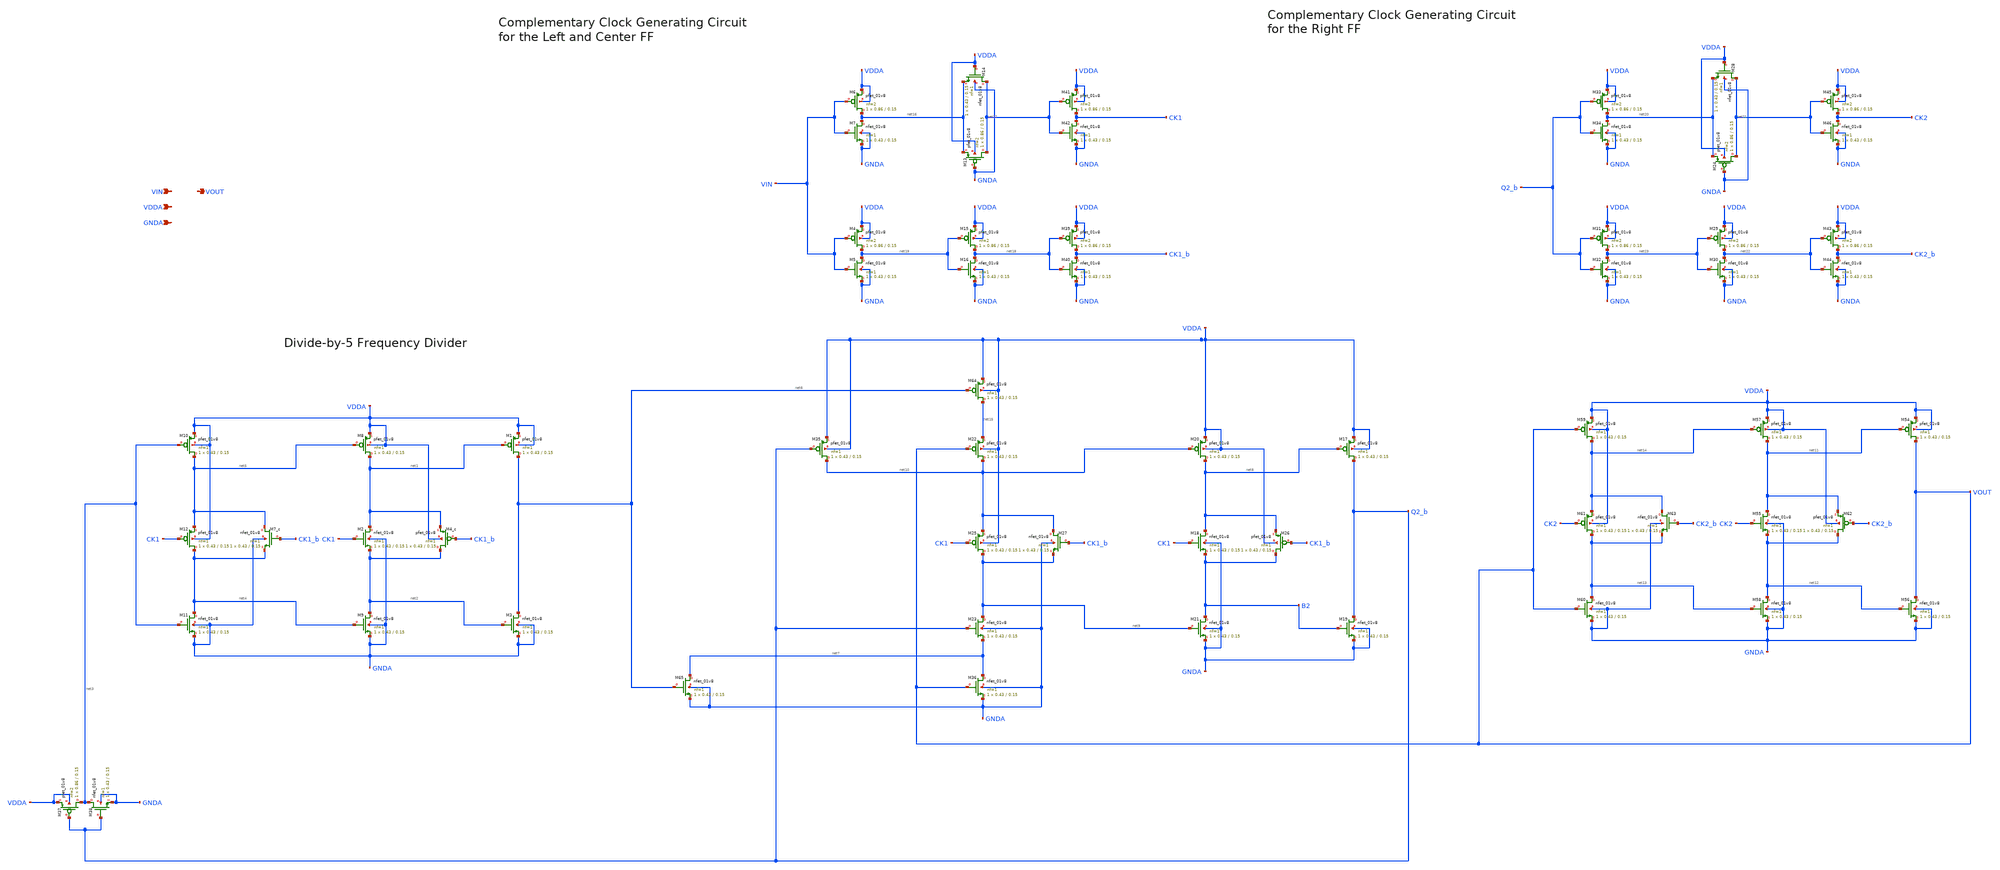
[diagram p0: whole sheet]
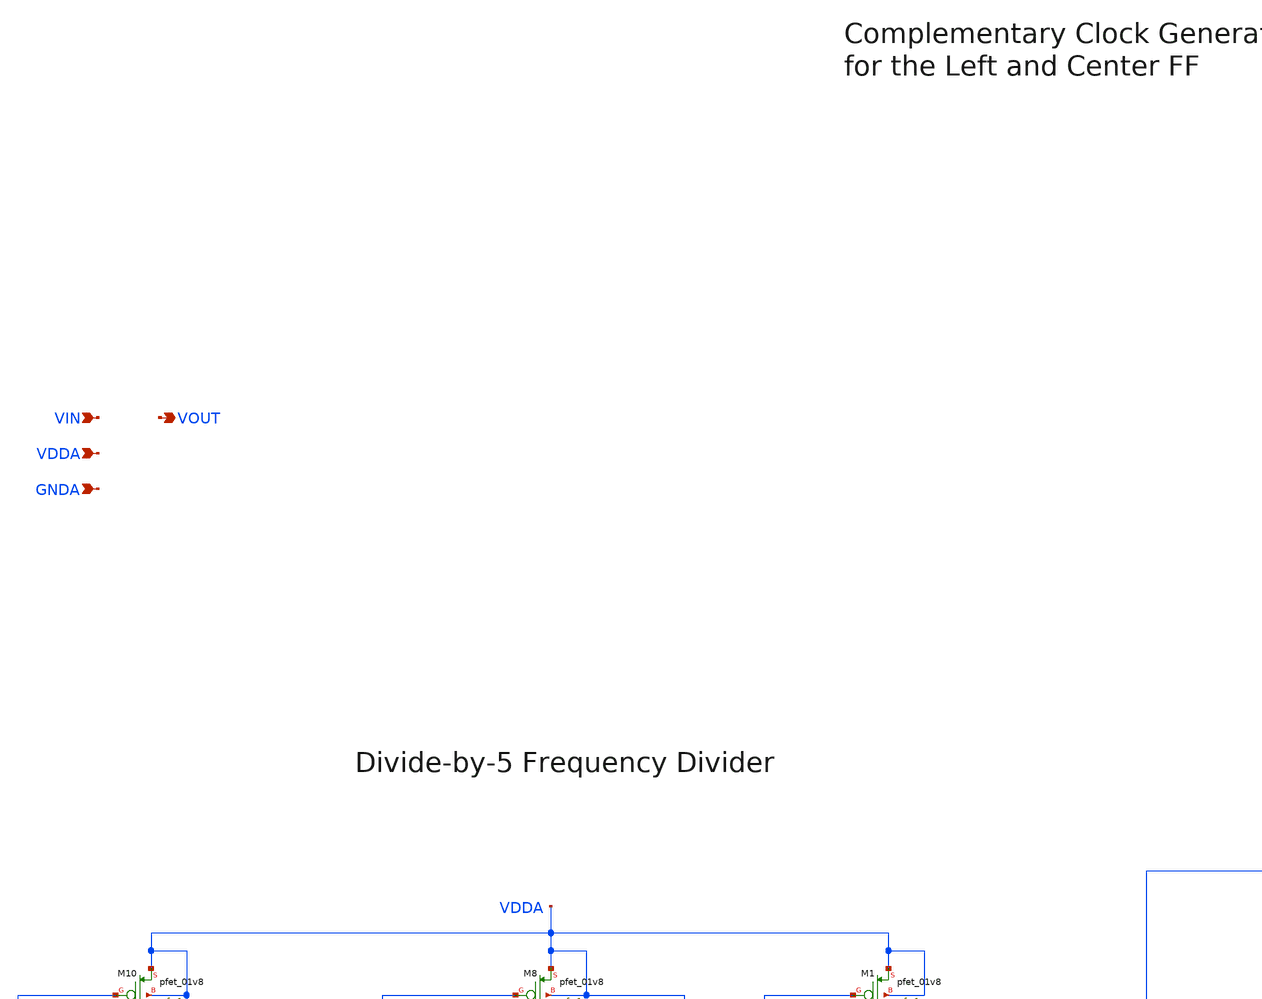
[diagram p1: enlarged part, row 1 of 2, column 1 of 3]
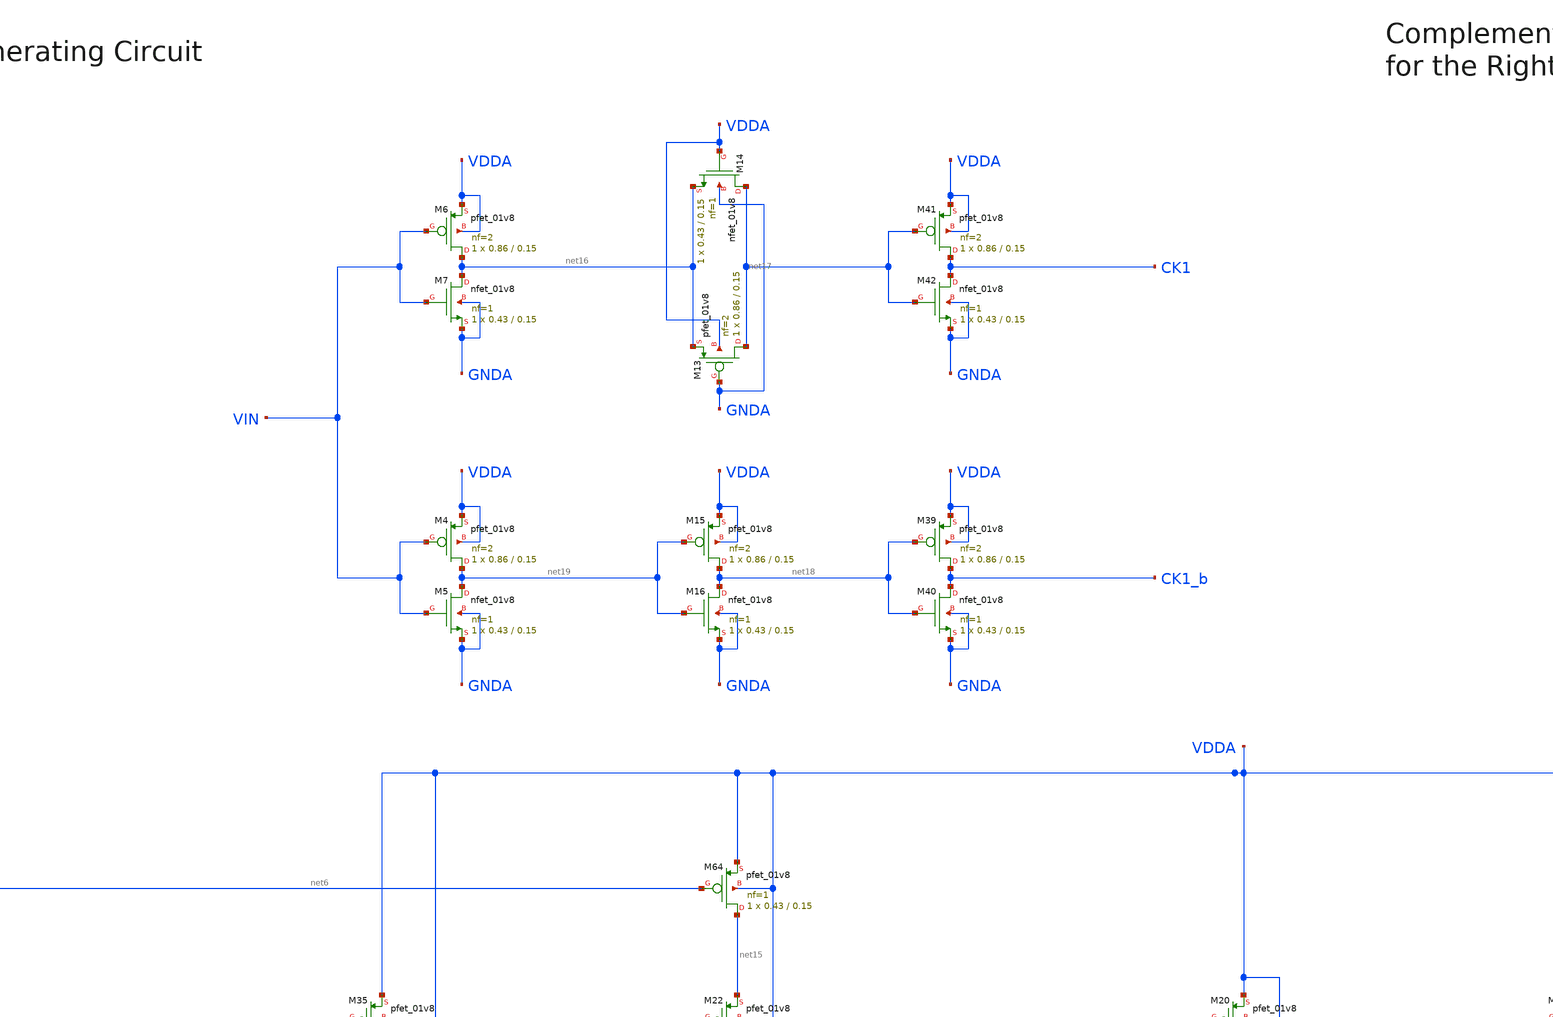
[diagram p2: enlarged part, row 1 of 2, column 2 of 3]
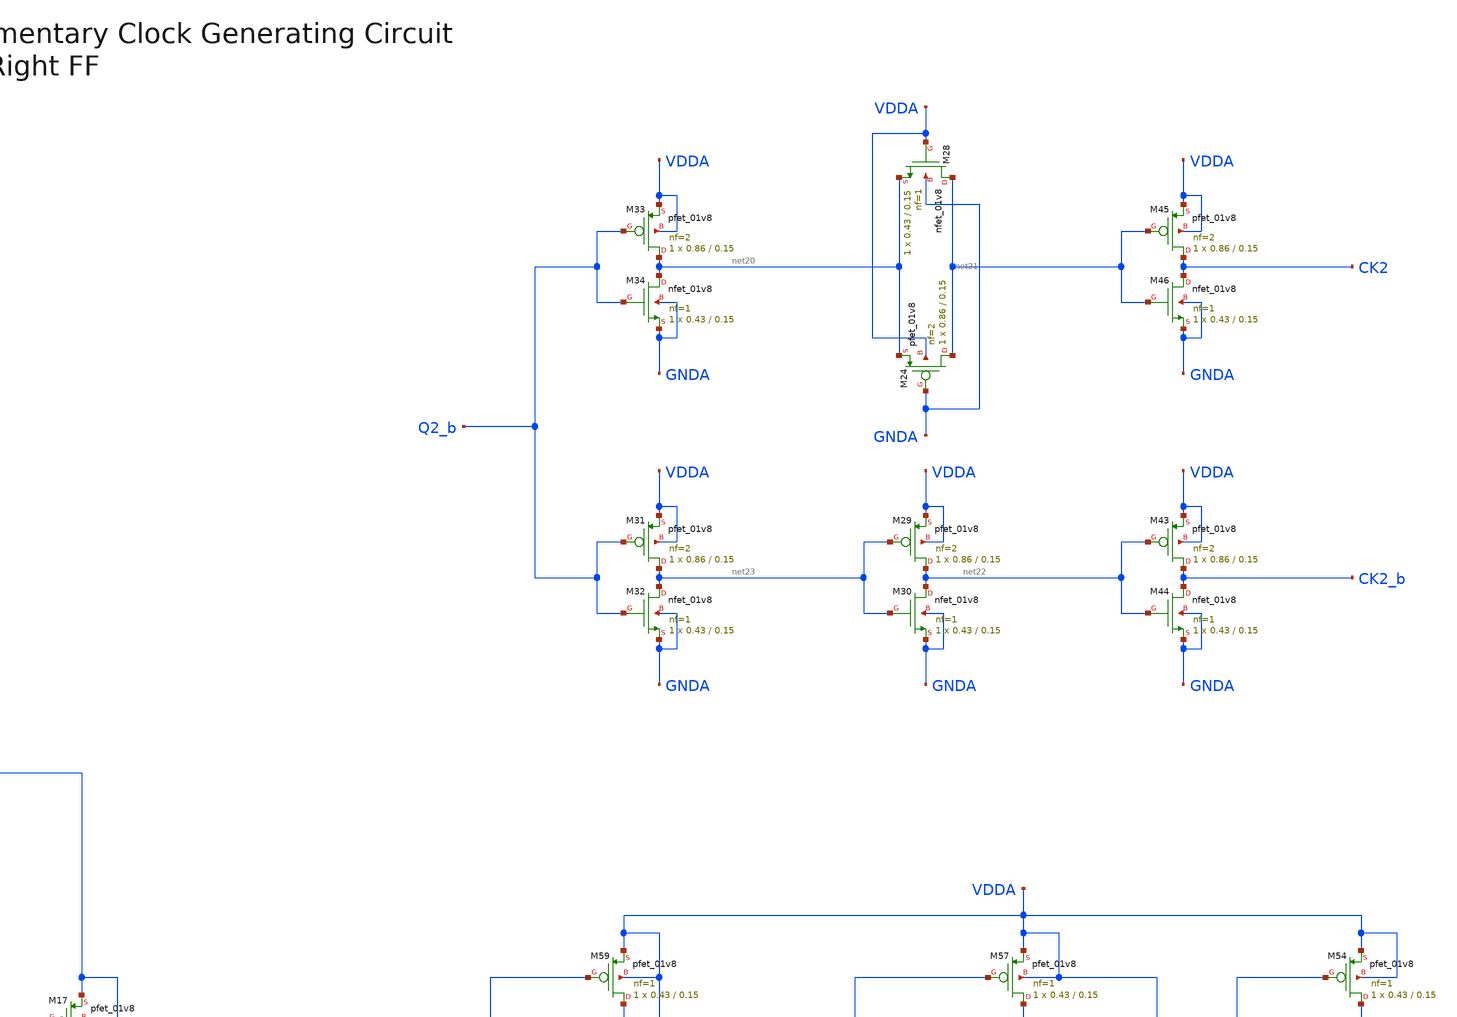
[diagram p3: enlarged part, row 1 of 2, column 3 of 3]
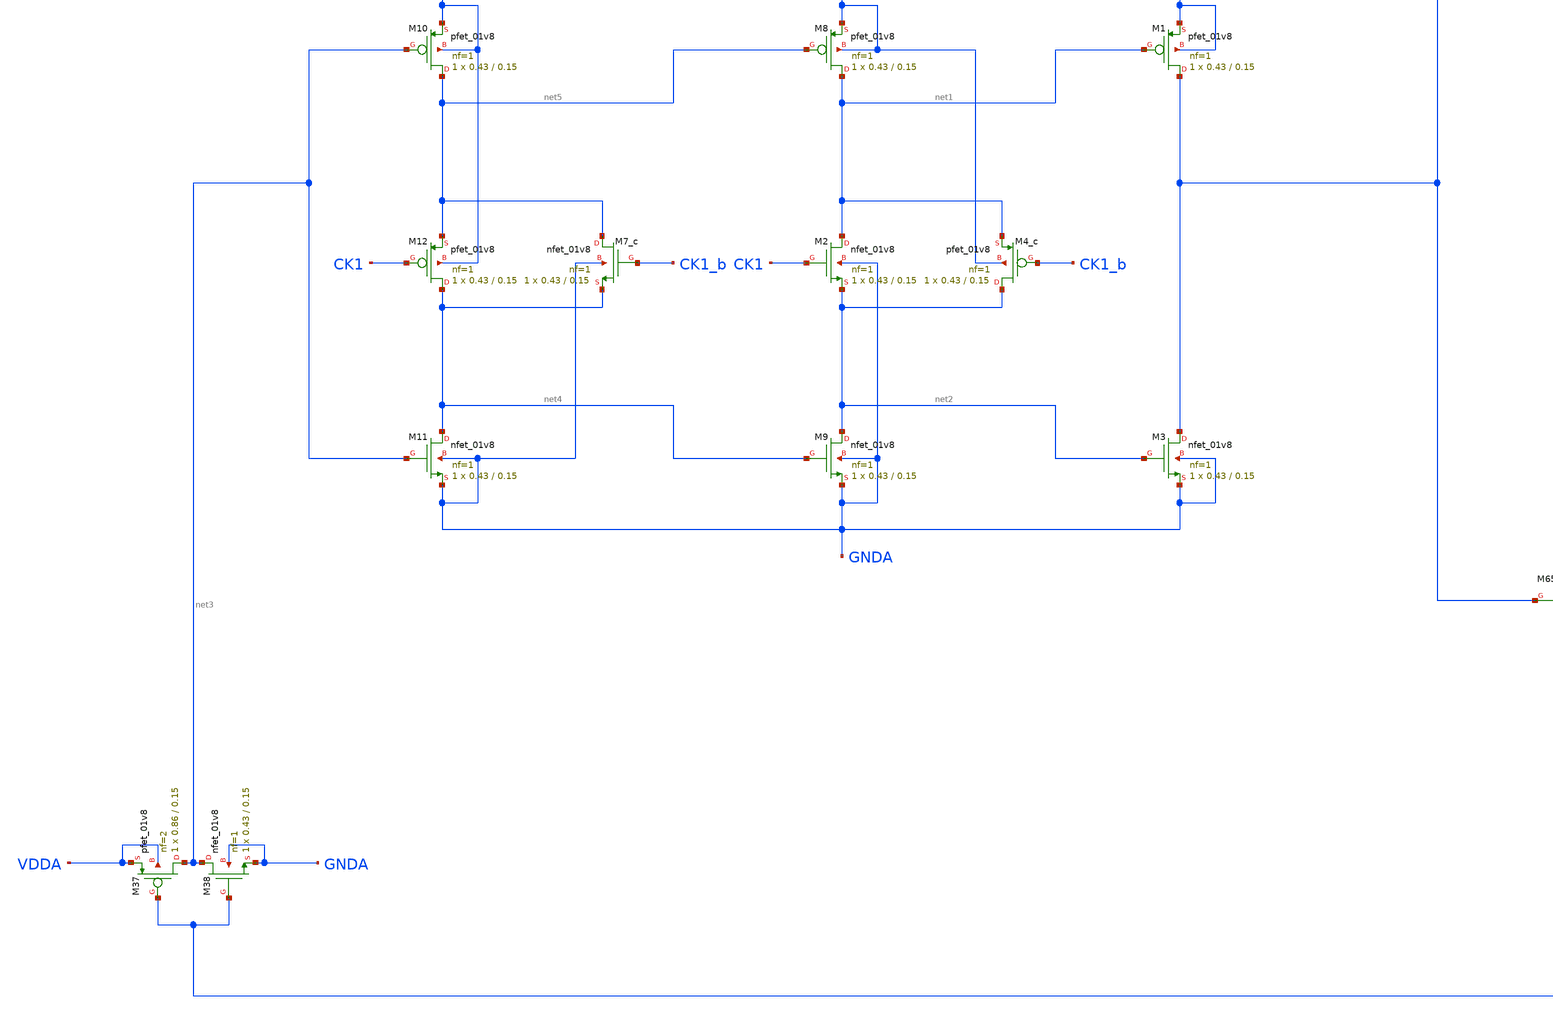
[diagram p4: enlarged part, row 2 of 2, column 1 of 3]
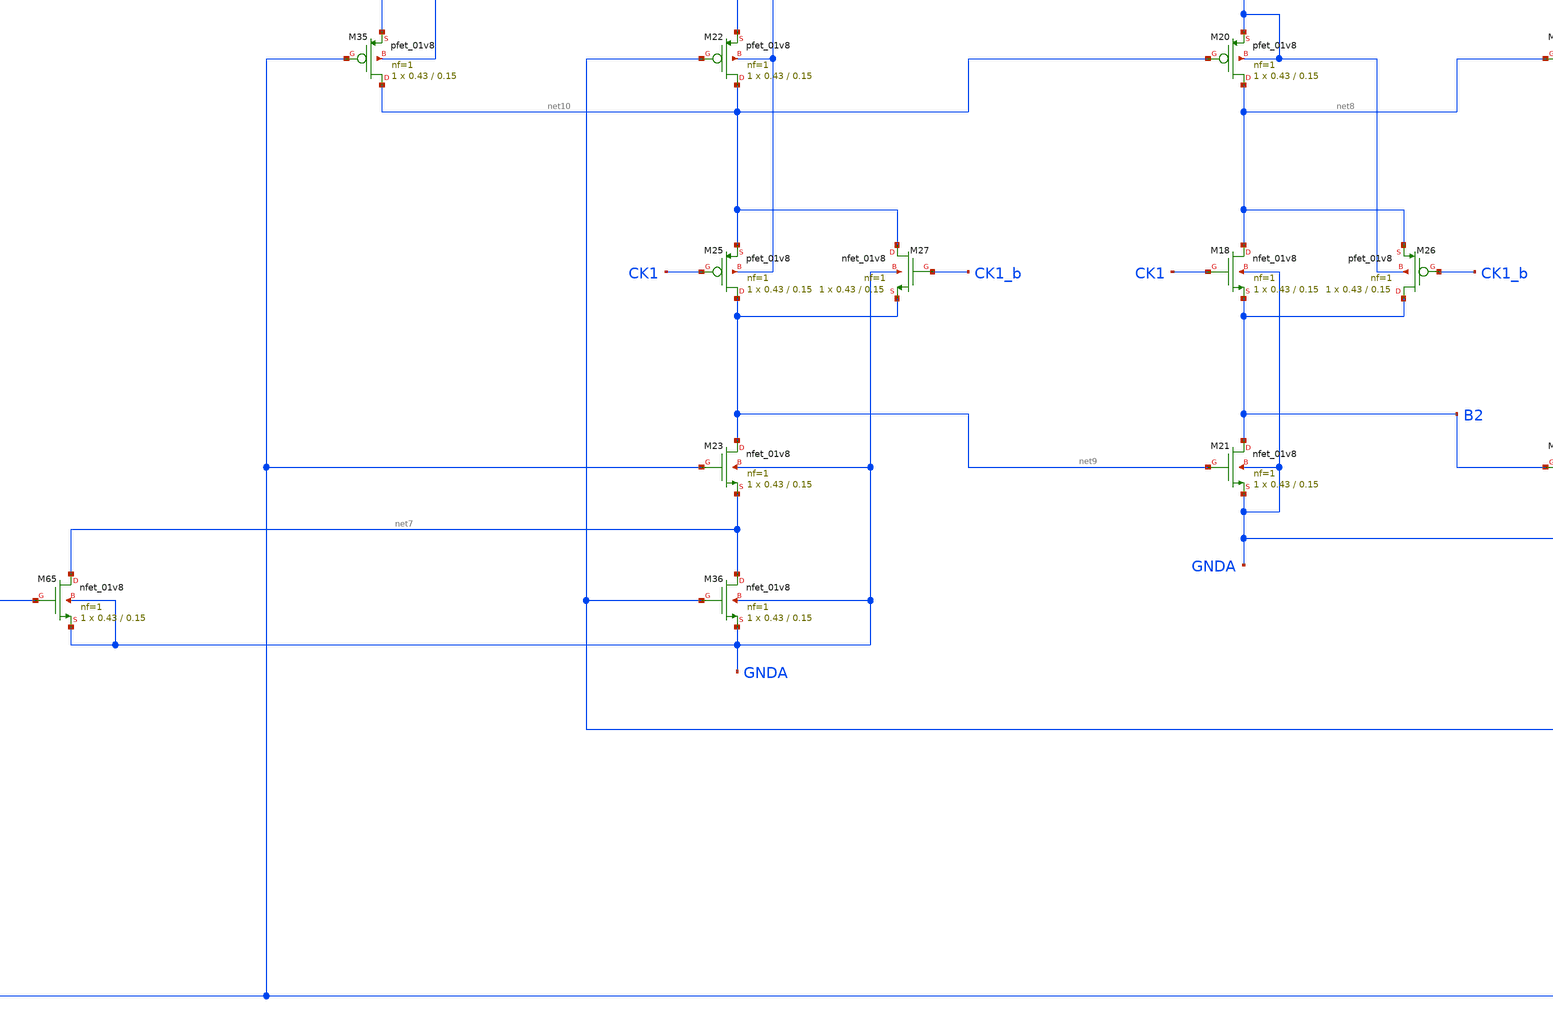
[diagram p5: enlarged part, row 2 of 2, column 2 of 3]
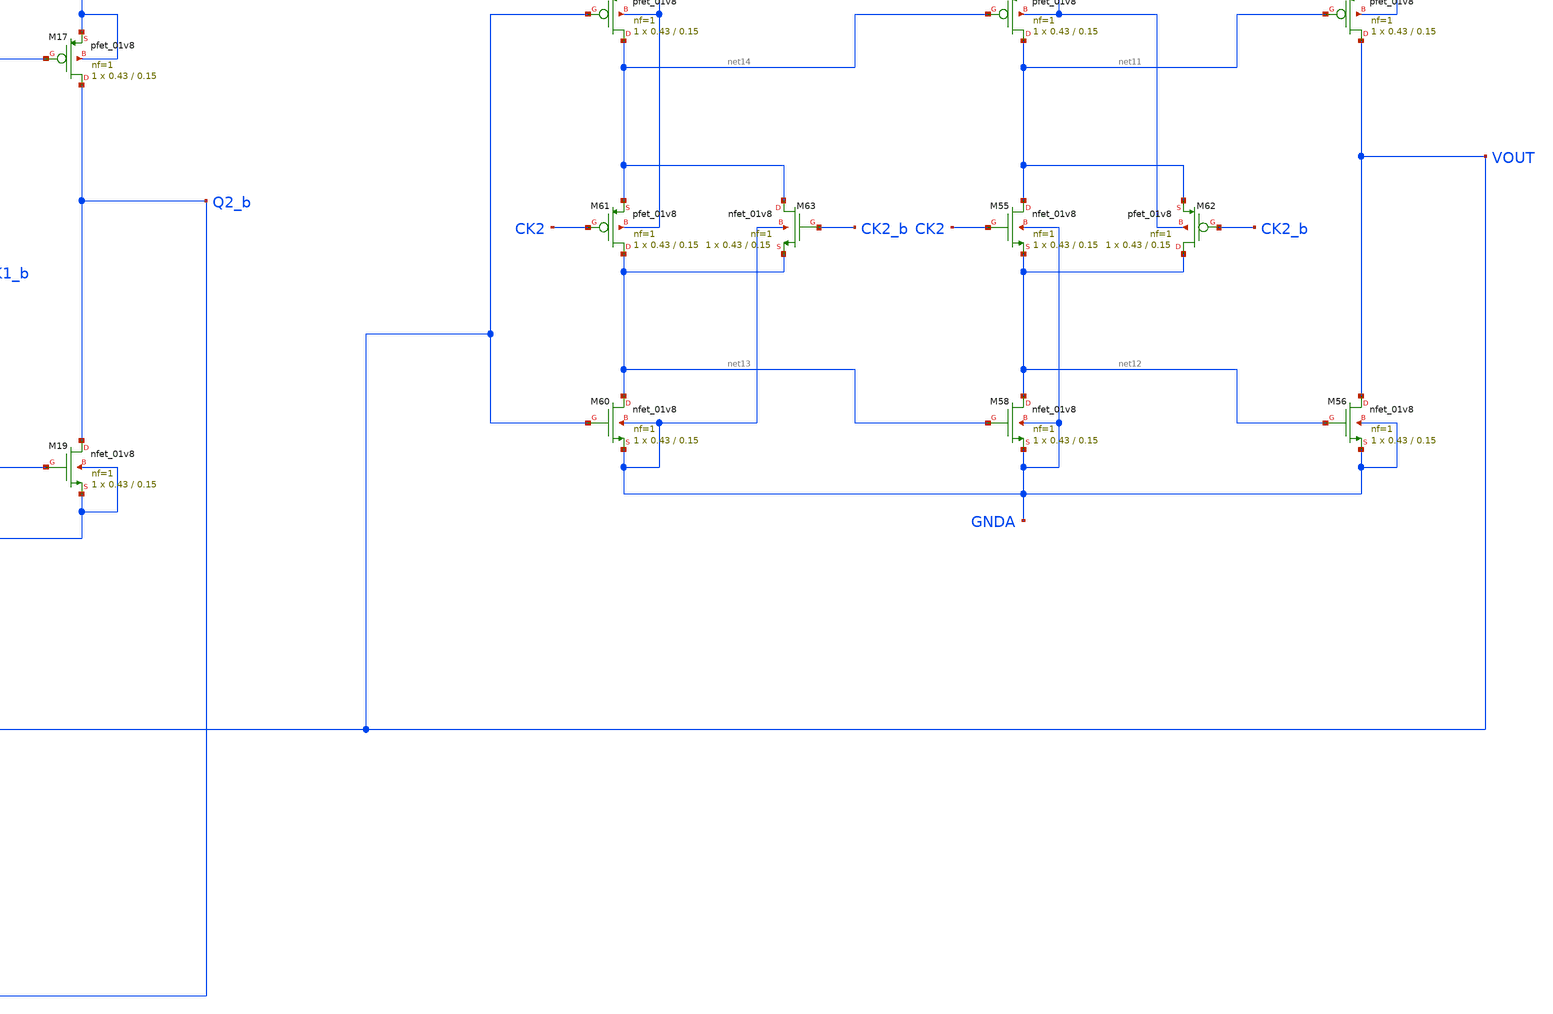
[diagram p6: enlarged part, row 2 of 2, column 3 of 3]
** sch_path: projects/pll/divider/xschem_ngspice/TSPC_FF_comp_sw_divide5.sch
**.subckt TSPC_FF_comp_sw_divide5 VIN VOUT VDDA GNDA
*.ipin VIN
*.opin VOUT
*.ipin VDDA
*.ipin GNDA
XM1 net6 net1 VDDA VDDA sky130_fd_pr__pfet_01v8 L=0.15 W=0.43 nf=1 ad='int((nf+1)/2) * W/nf * 0.29' as='int((nf+2)/2) * W/nf * 0.29'
+ pd='2*int((nf+1)/2) * (W/nf + 0.29)' ps='2*int((nf+2)/2) * (W/nf + 0.29)' nrd='0.29 / W' nrs='0.29 / W'
+ sa=0 sb=0 sd=0 mult=1 m=1
XM2 net1 CK1 net2 GNDA sky130_fd_pr__nfet_01v8 L=0.15 W=0.43 nf=1 ad='int((nf+1)/2) * W/nf * 0.29' as='int((nf+2)/2) * W/nf * 0.29'
+ pd='2*int((nf+1)/2) * (W/nf + 0.29)' ps='2*int((nf+2)/2) * (W/nf + 0.29)' nrd='0.29 / W' nrs='0.29 / W'
+ sa=0 sb=0 sd=0 mult=1 m=1
XM3 net6 net2 GNDA GNDA sky130_fd_pr__nfet_01v8 L=0.15 W=0.43 nf=1 ad='int((nf+1)/2) * W/nf * 0.29' as='int((nf+2)/2) * W/nf * 0.29'
+ pd='2*int((nf+1)/2) * (W/nf + 0.29)' ps='2*int((nf+2)/2) * (W/nf + 0.29)' nrd='0.29 / W' nrs='0.29 / W'
+ sa=0 sb=0 sd=0 mult=1 m=1
XM8 net1 net5 VDDA VDDA sky130_fd_pr__pfet_01v8 L=0.15 W=0.43 nf=1 ad='int((nf+1)/2) * W/nf * 0.29' as='int((nf+2)/2) * W/nf * 0.29'
+ pd='2*int((nf+1)/2) * (W/nf + 0.29)' ps='2*int((nf+2)/2) * (W/nf + 0.29)' nrd='0.29 / W' nrs='0.29 / W'
+ sa=0 sb=0 sd=0 mult=1 m=1
XM9 net2 net4 GNDA GNDA sky130_fd_pr__nfet_01v8 L=0.15 W=0.43 nf=1 ad='int((nf+1)/2) * W/nf * 0.29' as='int((nf+2)/2) * W/nf * 0.29'
+ pd='2*int((nf+1)/2) * (W/nf + 0.29)' ps='2*int((nf+2)/2) * (W/nf + 0.29)' nrd='0.29 / W' nrs='0.29 / W'
+ sa=0 sb=0 sd=0 mult=1 m=1
XM10 net5 net3 VDDA VDDA sky130_fd_pr__pfet_01v8 L=0.15 W=0.43 nf=1 ad='int((nf+1)/2) * W/nf * 0.29'
+ as='int((nf+2)/2) * W/nf * 0.29' pd='2*int((nf+1)/2) * (W/nf + 0.29)' ps='2*int((nf+2)/2) * (W/nf + 0.29)'
+ nrd='0.29 / W' nrs='0.29 / W' sa=0 sb=0 sd=0 mult=1 m=1
XM11 net4 net3 GNDA GNDA sky130_fd_pr__nfet_01v8 L=0.15 W=0.43 nf=1 ad='int((nf+1)/2) * W/nf * 0.29'
+ as='int((nf+2)/2) * W/nf * 0.29' pd='2*int((nf+1)/2) * (W/nf + 0.29)' ps='2*int((nf+2)/2) * (W/nf + 0.29)'
+ nrd='0.29 / W' nrs='0.29 / W' sa=0 sb=0 sd=0 mult=1 m=1
XM12 net4 CK1 net5 VDDA sky130_fd_pr__pfet_01v8 L=0.15 W=0.43 nf=1 ad='int((nf+1)/2) * W/nf * 0.29' as='int((nf+2)/2) * W/nf * 0.29'
+ pd='2*int((nf+1)/2) * (W/nf + 0.29)' ps='2*int((nf+2)/2) * (W/nf + 0.29)' nrd='0.29 / W' nrs='0.29 / W'
+ sa=0 sb=0 sd=0 mult=1 m=1
XM4_c net2 CK1_b net1 VDDA sky130_fd_pr__pfet_01v8 L=0.15 W=0.43 nf=1 ad='int((nf+1)/2) * W/nf * 0.29'
+ as='int((nf+2)/2) * W/nf * 0.29' pd='2*int((nf+1)/2) * (W/nf + 0.29)' ps='2*int((nf+2)/2) * (W/nf + 0.29)'
+ nrd='0.29 / W' nrs='0.29 / W' sa=0 sb=0 sd=0 mult=1 m=1
XM7_c net5 CK1_b net4 GNDA sky130_fd_pr__nfet_01v8 L=0.15 W=0.43 nf=1 ad='int((nf+1)/2) * W/nf * 0.29'
+ as='int((nf+2)/2) * W/nf * 0.29' pd='2*int((nf+1)/2) * (W/nf + 0.29)' ps='2*int((nf+2)/2) * (W/nf + 0.29)'
+ nrd='0.29 / W' nrs='0.29 / W' sa=0 sb=0 sd=0 mult=1 m=1
XM17 Q2_b net8 VDDA VDDA sky130_fd_pr__pfet_01v8 L=0.15 W=0.43 nf=1 ad='int((nf+1)/2) * W/nf * 0.29'
+ as='int((nf+2)/2) * W/nf * 0.29' pd='2*int((nf+1)/2) * (W/nf + 0.29)' ps='2*int((nf+2)/2) * (W/nf + 0.29)'
+ nrd='0.29 / W' nrs='0.29 / W' sa=0 sb=0 sd=0 mult=1 m=1
XM18 net8 CK1 B2 GNDA sky130_fd_pr__nfet_01v8 L=0.15 W=0.43 nf=1 ad='int((nf+1)/2) * W/nf * 0.29' as='int((nf+2)/2) * W/nf * 0.29'
+ pd='2*int((nf+1)/2) * (W/nf + 0.29)' ps='2*int((nf+2)/2) * (W/nf + 0.29)' nrd='0.29 / W' nrs='0.29 / W'
+ sa=0 sb=0 sd=0 mult=1 m=1
XM19 Q2_b B2 GNDA GNDA sky130_fd_pr__nfet_01v8 L=0.15 W=0.43 nf=1 ad='int((nf+1)/2) * W/nf * 0.29' as='int((nf+2)/2) * W/nf * 0.29'
+ pd='2*int((nf+1)/2) * (W/nf + 0.29)' ps='2*int((nf+2)/2) * (W/nf + 0.29)' nrd='0.29 / W' nrs='0.29 / W'
+ sa=0 sb=0 sd=0 mult=1 m=1
XM20 net8 net10 VDDA VDDA sky130_fd_pr__pfet_01v8 L=0.15 W=0.43 nf=1 ad='int((nf+1)/2) * W/nf * 0.29'
+ as='int((nf+2)/2) * W/nf * 0.29' pd='2*int((nf+1)/2) * (W/nf + 0.29)' ps='2*int((nf+2)/2) * (W/nf + 0.29)'
+ nrd='0.29 / W' nrs='0.29 / W' sa=0 sb=0 sd=0 mult=1 m=1
XM21 B2 net9 GNDA GNDA sky130_fd_pr__nfet_01v8 L=0.15 W=0.43 nf=1 ad='int((nf+1)/2) * W/nf * 0.29' as='int((nf+2)/2) * W/nf * 0.29'
+ pd='2*int((nf+1)/2) * (W/nf + 0.29)' ps='2*int((nf+2)/2) * (W/nf + 0.29)' nrd='0.29 / W' nrs='0.29 / W'
+ sa=0 sb=0 sd=0 mult=1 m=1
XM22 net10 VOUT net15 VDDA sky130_fd_pr__pfet_01v8 L=0.15 W=0.43 nf=1 ad='int((nf+1)/2) * W/nf * 0.29'
+ as='int((nf+2)/2) * W/nf * 0.29' pd='2*int((nf+1)/2) * (W/nf + 0.29)' ps='2*int((nf+2)/2) * (W/nf + 0.29)'
+ nrd='0.29 / W' nrs='0.29 / W' sa=0 sb=0 sd=0 mult=1 m=1
XM23 net9 Q2_b net7 GNDA sky130_fd_pr__nfet_01v8 L=0.15 W=0.43 nf=1 ad='int((nf+1)/2) * W/nf * 0.29'
+ as='int((nf+2)/2) * W/nf * 0.29' pd='2*int((nf+1)/2) * (W/nf + 0.29)' ps='2*int((nf+2)/2) * (W/nf + 0.29)'
+ nrd='0.29 / W' nrs='0.29 / W' sa=0 sb=0 sd=0 mult=1 m=1
XM25 net9 CK1 net10 VDDA sky130_fd_pr__pfet_01v8 L=0.15 W=0.43 nf=1 ad='int((nf+1)/2) * W/nf * 0.29'
+ as='int((nf+2)/2) * W/nf * 0.29' pd='2*int((nf+1)/2) * (W/nf + 0.29)' ps='2*int((nf+2)/2) * (W/nf + 0.29)'
+ nrd='0.29 / W' nrs='0.29 / W' sa=0 sb=0 sd=0 mult=1 m=1
XM26 B2 CK1_b net8 VDDA sky130_fd_pr__pfet_01v8 L=0.15 W=0.43 nf=1 ad='int((nf+1)/2) * W/nf * 0.29' as='int((nf+2)/2) * W/nf * 0.29'
+ pd='2*int((nf+1)/2) * (W/nf + 0.29)' ps='2*int((nf+2)/2) * (W/nf + 0.29)' nrd='0.29 / W' nrs='0.29 / W'
+ sa=0 sb=0 sd=0 mult=1 m=1
XM27 net10 CK1_b net9 GNDA sky130_fd_pr__nfet_01v8 L=0.15 W=0.43 nf=1 ad='int((nf+1)/2) * W/nf * 0.29'
+ as='int((nf+2)/2) * W/nf * 0.29' pd='2*int((nf+1)/2) * (W/nf + 0.29)' ps='2*int((nf+2)/2) * (W/nf + 0.29)'
+ nrd='0.29 / W' nrs='0.29 / W' sa=0 sb=0 sd=0 mult=1 m=1
XM35 net10 Q2_b VDDA VDDA sky130_fd_pr__pfet_01v8 L=0.15 W=0.43 nf=1 ad='int((nf+1)/2) * W/nf * 0.29'
+ as='int((nf+2)/2) * W/nf * 0.29' pd='2*int((nf+1)/2) * (W/nf + 0.29)' ps='2*int((nf+2)/2) * (W/nf + 0.29)'
+ nrd='0.29 / W' nrs='0.29 / W' sa=0 sb=0 sd=0 mult=1 m=1
XM36 net7 VOUT GNDA GNDA sky130_fd_pr__nfet_01v8 L=0.15 W=0.43 nf=1 ad='int((nf+1)/2) * W/nf * 0.29'
+ as='int((nf+2)/2) * W/nf * 0.29' pd='2*int((nf+1)/2) * (W/nf + 0.29)' ps='2*int((nf+2)/2) * (W/nf + 0.29)'
+ nrd='0.29 / W' nrs='0.29 / W' sa=0 sb=0 sd=0 mult=1 m=1
XM37 net3 Q2_b VDDA VDDA sky130_fd_pr__pfet_01v8 L=0.15 W=0.86 nf=2 ad='int((nf+1)/2) * W/nf * 0.29'
+ as='int((nf+2)/2) * W/nf * 0.29' pd='2*int((nf+1)/2) * (W/nf + 0.29)' ps='2*int((nf+2)/2) * (W/nf + 0.29)'
+ nrd='0.29 / W' nrs='0.29 / W' sa=0 sb=0 sd=0 mult=1 m=1
XM38 net3 Q2_b GNDA GNDA sky130_fd_pr__nfet_01v8 L=0.15 W=0.43 nf=1 ad='int((nf+1)/2) * W/nf * 0.29'
+ as='int((nf+2)/2) * W/nf * 0.29' pd='2*int((nf+1)/2) * (W/nf + 0.29)' ps='2*int((nf+2)/2) * (W/nf + 0.29)'
+ nrd='0.29 / W' nrs='0.29 / W' sa=0 sb=0 sd=0 mult=1 m=1
XM54 VOUT net11 VDDA VDDA sky130_fd_pr__pfet_01v8 L=0.15 W=0.43 nf=1 ad='int((nf+1)/2) * W/nf * 0.29'
+ as='int((nf+2)/2) * W/nf * 0.29' pd='2*int((nf+1)/2) * (W/nf + 0.29)' ps='2*int((nf+2)/2) * (W/nf + 0.29)'
+ nrd='0.29 / W' nrs='0.29 / W' sa=0 sb=0 sd=0 mult=1 m=1
XM55 net11 CK2 net12 GNDA sky130_fd_pr__nfet_01v8 L=0.15 W=0.43 nf=1 ad='int((nf+1)/2) * W/nf * 0.29'
+ as='int((nf+2)/2) * W/nf * 0.29' pd='2*int((nf+1)/2) * (W/nf + 0.29)' ps='2*int((nf+2)/2) * (W/nf + 0.29)'
+ nrd='0.29 / W' nrs='0.29 / W' sa=0 sb=0 sd=0 mult=1 m=1
XM56 VOUT net12 GNDA GNDA sky130_fd_pr__nfet_01v8 L=0.15 W=0.43 nf=1 ad='int((nf+1)/2) * W/nf * 0.29'
+ as='int((nf+2)/2) * W/nf * 0.29' pd='2*int((nf+1)/2) * (W/nf + 0.29)' ps='2*int((nf+2)/2) * (W/nf + 0.29)'
+ nrd='0.29 / W' nrs='0.29 / W' sa=0 sb=0 sd=0 mult=1 m=1
XM57 net11 net14 VDDA VDDA sky130_fd_pr__pfet_01v8 L=0.15 W=0.43 nf=1 ad='int((nf+1)/2) * W/nf * 0.29'
+ as='int((nf+2)/2) * W/nf * 0.29' pd='2*int((nf+1)/2) * (W/nf + 0.29)' ps='2*int((nf+2)/2) * (W/nf + 0.29)'
+ nrd='0.29 / W' nrs='0.29 / W' sa=0 sb=0 sd=0 mult=1 m=1
XM58 net12 net13 GNDA GNDA sky130_fd_pr__nfet_01v8 L=0.15 W=0.43 nf=1 ad='int((nf+1)/2) * W/nf * 0.29'
+ as='int((nf+2)/2) * W/nf * 0.29' pd='2*int((nf+1)/2) * (W/nf + 0.29)' ps='2*int((nf+2)/2) * (W/nf + 0.29)'
+ nrd='0.29 / W' nrs='0.29 / W' sa=0 sb=0 sd=0 mult=1 m=1
XM59 net14 VOUT VDDA VDDA sky130_fd_pr__pfet_01v8 L=0.15 W=0.43 nf=1 ad='int((nf+1)/2) * W/nf * 0.29'
+ as='int((nf+2)/2) * W/nf * 0.29' pd='2*int((nf+1)/2) * (W/nf + 0.29)' ps='2*int((nf+2)/2) * (W/nf + 0.29)'
+ nrd='0.29 / W' nrs='0.29 / W' sa=0 sb=0 sd=0 mult=1 m=1
XM60 net13 VOUT GNDA GNDA sky130_fd_pr__nfet_01v8 L=0.15 W=0.43 nf=1 ad='int((nf+1)/2) * W/nf * 0.29'
+ as='int((nf+2)/2) * W/nf * 0.29' pd='2*int((nf+1)/2) * (W/nf + 0.29)' ps='2*int((nf+2)/2) * (W/nf + 0.29)'
+ nrd='0.29 / W' nrs='0.29 / W' sa=0 sb=0 sd=0 mult=1 m=1
XM61 net13 CK2 net14 VDDA sky130_fd_pr__pfet_01v8 L=0.15 W=0.43 nf=1 ad='int((nf+1)/2) * W/nf * 0.29'
+ as='int((nf+2)/2) * W/nf * 0.29' pd='2*int((nf+1)/2) * (W/nf + 0.29)' ps='2*int((nf+2)/2) * (W/nf + 0.29)'
+ nrd='0.29 / W' nrs='0.29 / W' sa=0 sb=0 sd=0 mult=1 m=1
XM62 net12 CK2_b net11 VDDA sky130_fd_pr__pfet_01v8 L=0.15 W=0.43 nf=1 ad='int((nf+1)/2) * W/nf * 0.29'
+ as='int((nf+2)/2) * W/nf * 0.29' pd='2*int((nf+1)/2) * (W/nf + 0.29)' ps='2*int((nf+2)/2) * (W/nf + 0.29)'
+ nrd='0.29 / W' nrs='0.29 / W' sa=0 sb=0 sd=0 mult=1 m=1
XM63 net14 CK2_b net13 GNDA sky130_fd_pr__nfet_01v8 L=0.15 W=0.43 nf=1 ad='int((nf+1)/2) * W/nf * 0.29'
+ as='int((nf+2)/2) * W/nf * 0.29' pd='2*int((nf+1)/2) * (W/nf + 0.29)' ps='2*int((nf+2)/2) * (W/nf + 0.29)'
+ nrd='0.29 / W' nrs='0.29 / W' sa=0 sb=0 sd=0 mult=1 m=1
XM64 net15 net6 VDDA VDDA sky130_fd_pr__pfet_01v8 L=0.15 W=0.43 nf=1 ad='int((nf+1)/2) * W/nf * 0.29'
+ as='int((nf+2)/2) * W/nf * 0.29' pd='2*int((nf+1)/2) * (W/nf + 0.29)' ps='2*int((nf+2)/2) * (W/nf + 0.29)'
+ nrd='0.29 / W' nrs='0.29 / W' sa=0 sb=0 sd=0 mult=1 m=1
XM65 net7 net6 GNDA GNDA sky130_fd_pr__nfet_01v8 L=0.15 W=0.43 nf=1 ad='int((nf+1)/2) * W/nf * 0.29'
+ as='int((nf+2)/2) * W/nf * 0.29' pd='2*int((nf+1)/2) * (W/nf + 0.29)' ps='2*int((nf+2)/2) * (W/nf + 0.29)'
+ nrd='0.29 / W' nrs='0.29 / W' sa=0 sb=0 sd=0 mult=1 m=1
XM13 net17 GNDA net16 VDDA sky130_fd_pr__pfet_01v8 L=0.15 W=0.86 nf=2 ad='int((nf+1)/2) * W/nf * 0.29'
+ as='int((nf+2)/2) * W/nf * 0.29' pd='2*int((nf+1)/2) * (W/nf + 0.29)' ps='2*int((nf+2)/2) * (W/nf + 0.29)'
+ nrd='0.29 / W' nrs='0.29 / W' sa=0 sb=0 sd=0 mult=1 m=1
XM14 net17 VDDA net16 GNDA sky130_fd_pr__nfet_01v8 L=0.15 W=0.43 nf=1 ad='int((nf+1)/2) * W/nf * 0.29'
+ as='int((nf+2)/2) * W/nf * 0.29' pd='2*int((nf+1)/2) * (W/nf + 0.29)' ps='2*int((nf+2)/2) * (W/nf + 0.29)'
+ nrd='0.29 / W' nrs='0.29 / W' sa=0 sb=0 sd=0 mult=1 m=1
XM15 net18 net19 VDDA VDDA sky130_fd_pr__pfet_01v8 L=0.15 W=0.86 nf=2 ad='int((nf+1)/2) * W/nf * 0.29'
+ as='int((nf+2)/2) * W/nf * 0.29' pd='2*int((nf+1)/2) * (W/nf + 0.29)' ps='2*int((nf+2)/2) * (W/nf + 0.29)'
+ nrd='0.29 / W' nrs='0.29 / W' sa=0 sb=0 sd=0 mult=1 m=1
XM16 net18 net19 GNDA GNDA sky130_fd_pr__nfet_01v8 L=0.15 W=0.43 nf=1 ad='int((nf+1)/2) * W/nf * 0.29'
+ as='int((nf+2)/2) * W/nf * 0.29' pd='2*int((nf+1)/2) * (W/nf + 0.29)' ps='2*int((nf+2)/2) * (W/nf + 0.29)'
+ nrd='0.29 / W' nrs='0.29 / W' sa=0 sb=0 sd=0 mult=1 m=1
XM24 net21 GNDA net20 VDDA sky130_fd_pr__pfet_01v8 L=0.15 W=0.86 nf=2 ad='int((nf+1)/2) * W/nf * 0.29'
+ as='int((nf+2)/2) * W/nf * 0.29' pd='2*int((nf+1)/2) * (W/nf + 0.29)' ps='2*int((nf+2)/2) * (W/nf + 0.29)'
+ nrd='0.29 / W' nrs='0.29 / W' sa=0 sb=0 sd=0 mult=1 m=1
XM28 net21 VDDA net20 GNDA sky130_fd_pr__nfet_01v8 L=0.15 W=0.43 nf=1 ad='int((nf+1)/2) * W/nf * 0.29'
+ as='int((nf+2)/2) * W/nf * 0.29' pd='2*int((nf+1)/2) * (W/nf + 0.29)' ps='2*int((nf+2)/2) * (W/nf + 0.29)'
+ nrd='0.29 / W' nrs='0.29 / W' sa=0 sb=0 sd=0 mult=1 m=1
XM4 net19 VIN VDDA VDDA sky130_fd_pr__pfet_01v8 L=0.15 W=0.86 nf=2 ad='int((nf+1)/2) * W/nf * 0.29' as='int((nf+2)/2) * W/nf * 0.29'
+ pd='2*int((nf+1)/2) * (W/nf + 0.29)' ps='2*int((nf+2)/2) * (W/nf + 0.29)' nrd='0.29 / W' nrs='0.29 / W'
+ sa=0 sb=0 sd=0 mult=1 m=1
XM5 net19 VIN GNDA GNDA sky130_fd_pr__nfet_01v8 L=0.15 W=0.43 nf=1 ad='int((nf+1)/2) * W/nf * 0.29' as='int((nf+2)/2) * W/nf * 0.29'
+ pd='2*int((nf+1)/2) * (W/nf + 0.29)' ps='2*int((nf+2)/2) * (W/nf + 0.29)' nrd='0.29 / W' nrs='0.29 / W'
+ sa=0 sb=0 sd=0 mult=1 m=1
XM6 net16 VIN VDDA VDDA sky130_fd_pr__pfet_01v8 L=0.15 W=0.86 nf=2 ad='int((nf+1)/2) * W/nf * 0.29' as='int((nf+2)/2) * W/nf * 0.29'
+ pd='2*int((nf+1)/2) * (W/nf + 0.29)' ps='2*int((nf+2)/2) * (W/nf + 0.29)' nrd='0.29 / W' nrs='0.29 / W'
+ sa=0 sb=0 sd=0 mult=1 m=1
XM7 net16 VIN GNDA GNDA sky130_fd_pr__nfet_01v8 L=0.15 W=0.43 nf=1 ad='int((nf+1)/2) * W/nf * 0.29' as='int((nf+2)/2) * W/nf * 0.29'
+ pd='2*int((nf+1)/2) * (W/nf + 0.29)' ps='2*int((nf+2)/2) * (W/nf + 0.29)' nrd='0.29 / W' nrs='0.29 / W'
+ sa=0 sb=0 sd=0 mult=1 m=1
XM31 net23 Q2_b VDDA VDDA sky130_fd_pr__pfet_01v8 L=0.15 W=0.86 nf=2 ad='int((nf+1)/2) * W/nf * 0.29'
+ as='int((nf+2)/2) * W/nf * 0.29' pd='2*int((nf+1)/2) * (W/nf + 0.29)' ps='2*int((nf+2)/2) * (W/nf + 0.29)'
+ nrd='0.29 / W' nrs='0.29 / W' sa=0 sb=0 sd=0 mult=1 m=1
XM32 net23 Q2_b GNDA GNDA sky130_fd_pr__nfet_01v8 L=0.15 W=0.43 nf=1 ad='int((nf+1)/2) * W/nf * 0.29'
+ as='int((nf+2)/2) * W/nf * 0.29' pd='2*int((nf+1)/2) * (W/nf + 0.29)' ps='2*int((nf+2)/2) * (W/nf + 0.29)'
+ nrd='0.29 / W' nrs='0.29 / W' sa=0 sb=0 sd=0 mult=1 m=1
XM33 net20 Q2_b VDDA VDDA sky130_fd_pr__pfet_01v8 L=0.15 W=0.86 nf=2 ad='int((nf+1)/2) * W/nf * 0.29'
+ as='int((nf+2)/2) * W/nf * 0.29' pd='2*int((nf+1)/2) * (W/nf + 0.29)' ps='2*int((nf+2)/2) * (W/nf + 0.29)'
+ nrd='0.29 / W' nrs='0.29 / W' sa=0 sb=0 sd=0 mult=1 m=1
XM34 net20 Q2_b GNDA GNDA sky130_fd_pr__nfet_01v8 L=0.15 W=0.43 nf=1 ad='int((nf+1)/2) * W/nf * 0.29'
+ as='int((nf+2)/2) * W/nf * 0.29' pd='2*int((nf+1)/2) * (W/nf + 0.29)' ps='2*int((nf+2)/2) * (W/nf + 0.29)'
+ nrd='0.29 / W' nrs='0.29 / W' sa=0 sb=0 sd=0 mult=1 m=1
XM39 CK1_b net18 VDDA VDDA sky130_fd_pr__pfet_01v8 L=0.15 W=0.86 nf=2 ad='int((nf+1)/2) * W/nf * 0.29'
+ as='int((nf+2)/2) * W/nf * 0.29' pd='2*int((nf+1)/2) * (W/nf + 0.29)' ps='2*int((nf+2)/2) * (W/nf + 0.29)'
+ nrd='0.29 / W' nrs='0.29 / W' sa=0 sb=0 sd=0 mult=1 m=1
XM40 CK1_b net18 GNDA GNDA sky130_fd_pr__nfet_01v8 L=0.15 W=0.43 nf=1 ad='int((nf+1)/2) * W/nf * 0.29'
+ as='int((nf+2)/2) * W/nf * 0.29' pd='2*int((nf+1)/2) * (W/nf + 0.29)' ps='2*int((nf+2)/2) * (W/nf + 0.29)'
+ nrd='0.29 / W' nrs='0.29 / W' sa=0 sb=0 sd=0 mult=1 m=1
XM41 CK1 net17 VDDA VDDA sky130_fd_pr__pfet_01v8 L=0.15 W=0.86 nf=2 ad='int((nf+1)/2) * W/nf * 0.29'
+ as='int((nf+2)/2) * W/nf * 0.29' pd='2*int((nf+1)/2) * (W/nf + 0.29)' ps='2*int((nf+2)/2) * (W/nf + 0.29)'
+ nrd='0.29 / W' nrs='0.29 / W' sa=0 sb=0 sd=0 mult=1 m=1
XM42 CK1 net17 GNDA GNDA sky130_fd_pr__nfet_01v8 L=0.15 W=0.43 nf=1 ad='int((nf+1)/2) * W/nf * 0.29'
+ as='int((nf+2)/2) * W/nf * 0.29' pd='2*int((nf+1)/2) * (W/nf + 0.29)' ps='2*int((nf+2)/2) * (W/nf + 0.29)'
+ nrd='0.29 / W' nrs='0.29 / W' sa=0 sb=0 sd=0 mult=1 m=1
XM43 CK2_b net22 VDDA VDDA sky130_fd_pr__pfet_01v8 L=0.15 W=0.86 nf=2 ad='int((nf+1)/2) * W/nf * 0.29'
+ as='int((nf+2)/2) * W/nf * 0.29' pd='2*int((nf+1)/2) * (W/nf + 0.29)' ps='2*int((nf+2)/2) * (W/nf + 0.29)'
+ nrd='0.29 / W' nrs='0.29 / W' sa=0 sb=0 sd=0 mult=1 m=1
XM44 CK2_b net22 GNDA GNDA sky130_fd_pr__nfet_01v8 L=0.15 W=0.43 nf=1 ad='int((nf+1)/2) * W/nf * 0.29'
+ as='int((nf+2)/2) * W/nf * 0.29' pd='2*int((nf+1)/2) * (W/nf + 0.29)' ps='2*int((nf+2)/2) * (W/nf + 0.29)'
+ nrd='0.29 / W' nrs='0.29 / W' sa=0 sb=0 sd=0 mult=1 m=1
XM45 CK2 net21 VDDA VDDA sky130_fd_pr__pfet_01v8 L=0.15 W=0.86 nf=2 ad='int((nf+1)/2) * W/nf * 0.29'
+ as='int((nf+2)/2) * W/nf * 0.29' pd='2*int((nf+1)/2) * (W/nf + 0.29)' ps='2*int((nf+2)/2) * (W/nf + 0.29)'
+ nrd='0.29 / W' nrs='0.29 / W' sa=0 sb=0 sd=0 mult=1 m=1
XM46 CK2 net21 GNDA GNDA sky130_fd_pr__nfet_01v8 L=0.15 W=0.43 nf=1 ad='int((nf+1)/2) * W/nf * 0.29'
+ as='int((nf+2)/2) * W/nf * 0.29' pd='2*int((nf+1)/2) * (W/nf + 0.29)' ps='2*int((nf+2)/2) * (W/nf + 0.29)'
+ nrd='0.29 / W' nrs='0.29 / W' sa=0 sb=0 sd=0 mult=1 m=1
XM29 net22 net23 VDDA VDDA sky130_fd_pr__pfet_01v8 L=0.15 W=0.86 nf=2 ad='int((nf+1)/2) * W/nf * 0.29'
+ as='int((nf+2)/2) * W/nf * 0.29' pd='2*int((nf+1)/2) * (W/nf + 0.29)' ps='2*int((nf+2)/2) * (W/nf + 0.29)'
+ nrd='0.29 / W' nrs='0.29 / W' sa=0 sb=0 sd=0 mult=1 m=1
XM30 net22 net23 GNDA GNDA sky130_fd_pr__nfet_01v8 L=0.15 W=0.43 nf=1 ad='int((nf+1)/2) * W/nf * 0.29'
+ as='int((nf+2)/2) * W/nf * 0.29' pd='2*int((nf+1)/2) * (W/nf + 0.29)' ps='2*int((nf+2)/2) * (W/nf + 0.29)'
+ nrd='0.29 / W' nrs='0.29 / W' sa=0 sb=0 sd=0 mult=1 m=1
**.ends
.end
